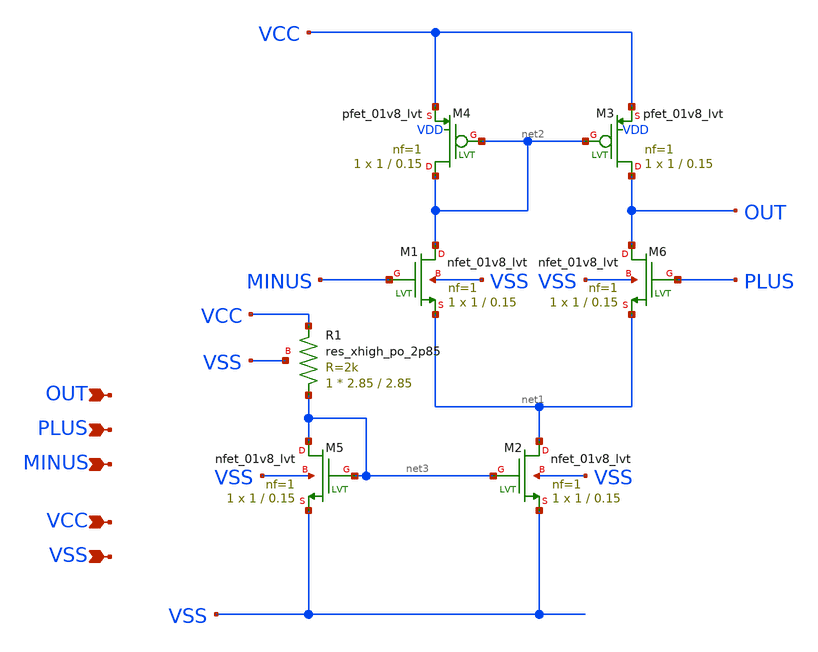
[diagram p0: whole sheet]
** sch_path: xschem/opamp_test.sch
**.subckt opamp_test OUT PLUS MINUS VCC VSS
*.ipin OUT
*.ipin PLUS
*.ipin MINUS
*.ipin VCC
*.ipin VSS
XR1 net3 VCC VSS sky130_fd_pr__res_xhigh_po_2p85 L=2.85 mult=1 m=1
XM1 net2 MINUS net1 VSS sky130_fd_pr__nfet_01v8_lvt L=0.15 W=1 nf=1 ad='int((nf+1)/2) * W/nf * 0.29'
+ as='int((nf+2)/2) * W/nf * 0.29' pd='2*int((nf+1)/2) * (W/nf + 0.29)' ps='2*int((nf+2)/2) * (W/nf + 0.29)'
+ nrd='0.29 / W' nrs='0.29 / W' sa=0 sb=0 sd=0 mult=1 m=1
XM2 net1 net3 VSS VSS sky130_fd_pr__nfet_01v8_lvt L=0.15 W=1 nf=1 ad='int((nf+1)/2) * W/nf * 0.29' as='int((nf+2)/2) * W/nf * 0.29'
+ pd='2*int((nf+1)/2) * (W/nf + 0.29)' ps='2*int((nf+2)/2) * (W/nf + 0.29)' nrd='0.29 / W' nrs='0.29 / W'
+ sa=0 sb=0 sd=0 mult=1 m=1
XM5 net3 net3 VSS VSS sky130_fd_pr__nfet_01v8_lvt L=0.15 W=1 nf=1 ad='int((nf+1)/2) * W/nf * 0.29' as='int((nf+2)/2) * W/nf * 0.29'
+ pd='2*int((nf+1)/2) * (W/nf + 0.29)' ps='2*int((nf+2)/2) * (W/nf + 0.29)' nrd='0.29 / W' nrs='0.29 / W'
+ sa=0 sb=0 sd=0 mult=1 m=1
XM6 OUT PLUS net1 VSS sky130_fd_pr__nfet_01v8_lvt L=0.15 W=1 nf=1 ad='int((nf+1)/2) * W/nf * 0.29' as='int((nf+2)/2) * W/nf * 0.29'
+ pd='2*int((nf+1)/2) * (W/nf + 0.29)' ps='2*int((nf+2)/2) * (W/nf + 0.29)' nrd='0.29 / W' nrs='0.29 / W'
+ sa=0 sb=0 sd=0 mult=1 m=1
XM3 OUT net2 VCC VDD sky130_fd_pr__pfet_01v8_lvt L=0.15 W=1 nf=1 ad='int((nf+1)/2) * W/nf * 0.29' as='int((nf+2)/2) * W/nf * 0.29'
+ pd='2*int((nf+1)/2) * (W/nf + 0.29)' ps='2*int((nf+2)/2) * (W/nf + 0.29)' nrd='0.29 / W' nrs='0.29 / W'
+ sa=0 sb=0 sd=0 mult=1 m=1
XM4 net2 net2 VCC VDD sky130_fd_pr__pfet_01v8_lvt L=0.15 W=1 nf=1 ad='int((nf+1)/2) * W/nf * 0.29' as='int((nf+2)/2) * W/nf * 0.29'
+ pd='2*int((nf+1)/2) * (W/nf + 0.29)' ps='2*int((nf+2)/2) * (W/nf + 0.29)' nrd='0.29 / W' nrs='0.29 / W'
+ sa=0 sb=0 sd=0 mult=1 m=1
**.ends
.end
